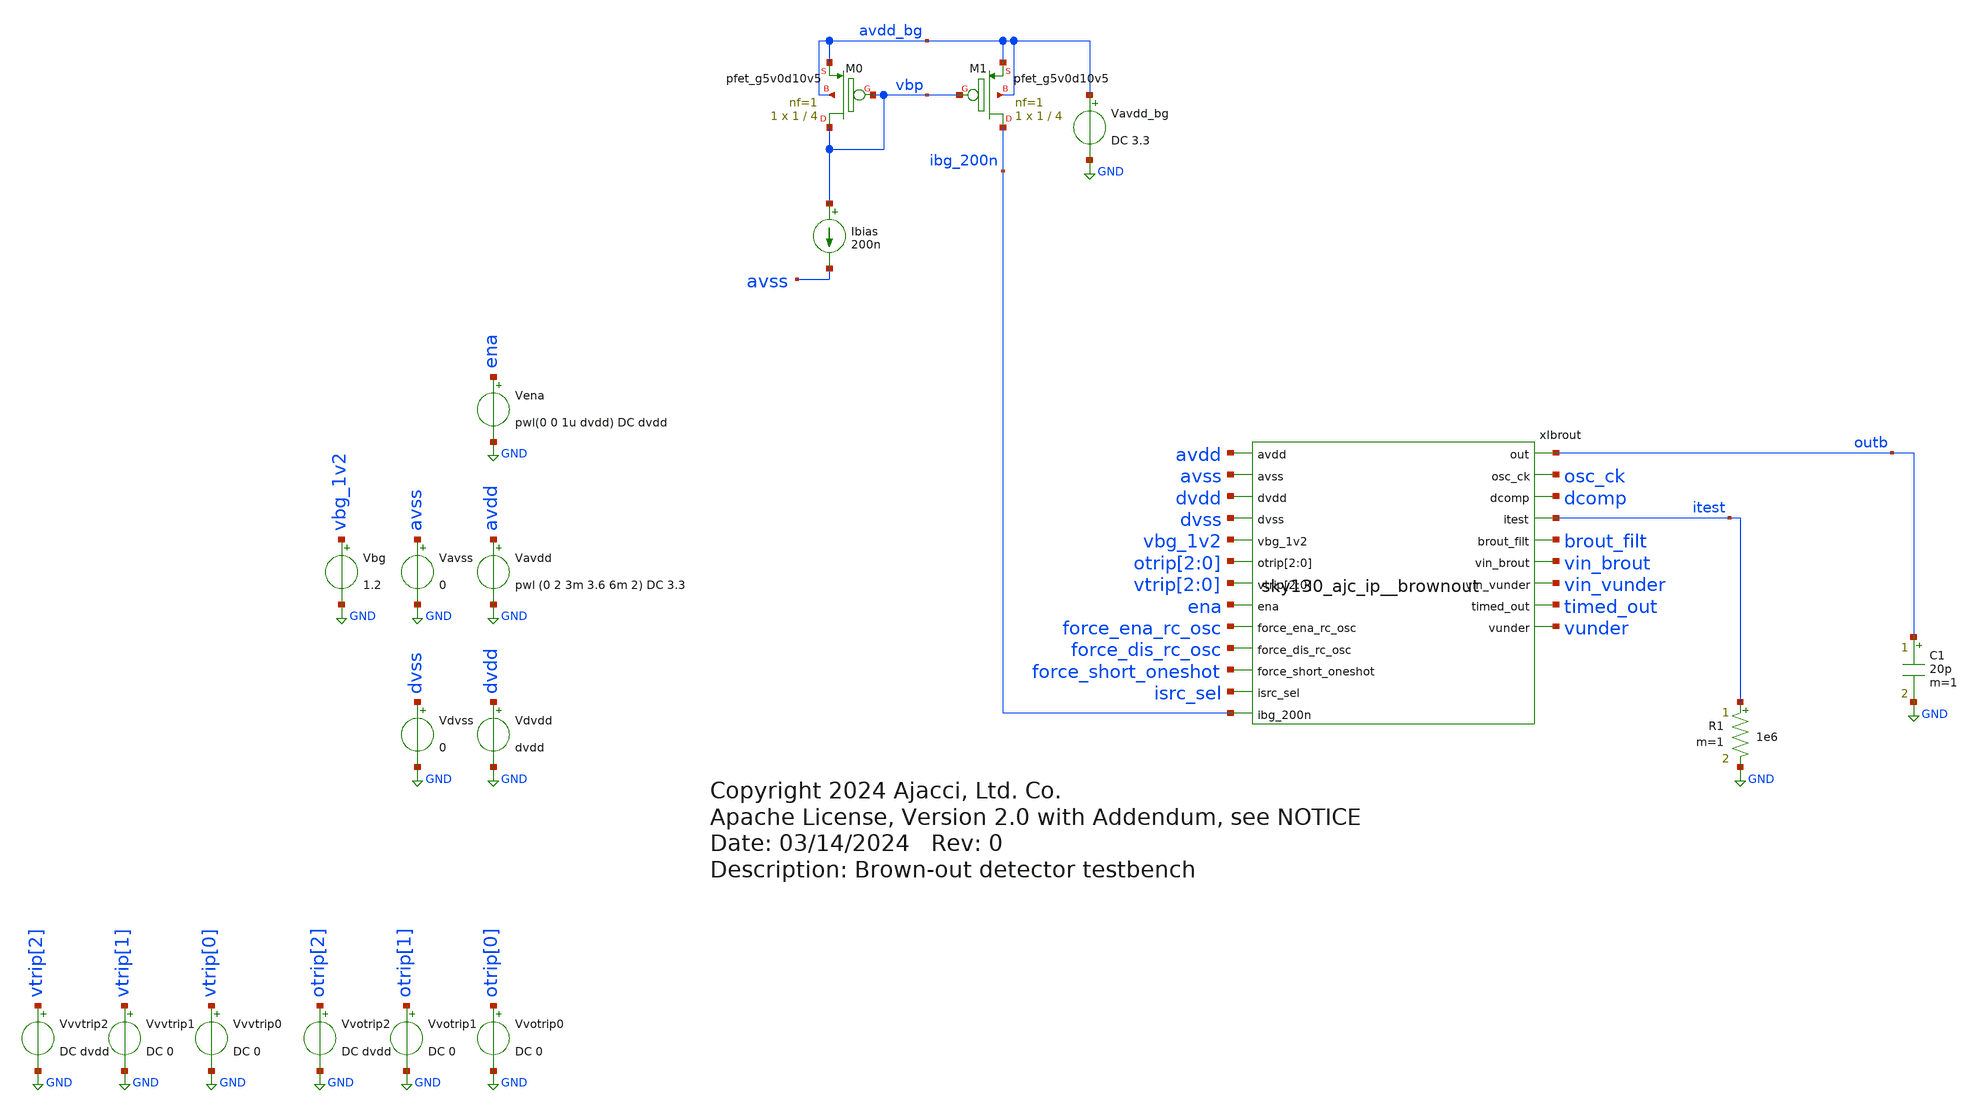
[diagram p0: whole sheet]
** sch_path: xschem/sky130_ajc_ip__brownout_tb.sch
* Copyright 2024 Ajacci, Ltd. Co.
* Apache License, Version 2.0 with Addendum, see NOTICE
**.subckt sky130_ajc_ip__brownout_tb
Vavss avss GND 0
Vena ena GND pwl(0 0 1u dvdd) DC dvdd
Vavdd avdd GND pwl (0 2 3m 3.6 6m 2) DC 3.3
.save i(vavdd)
Vbg vbg_1v2 GND 1.2
Ibias vbp avss 200n
XM1 ibg_200n vbp avdd_bg avdd_bg sky130_fd_pr__pfet_g5v0d10v5 L=4 W=1 nf=1 ad='int((nf+1)/2) * W/nf * 0.29'
+ as='int((nf+2)/2) * W/nf * 0.29' pd='2*int((nf+1)/2) * (W/nf + 0.29)' ps='2*int((nf+2)/2) * (W/nf + 0.29)'
+ nrd='0.29 / W' nrs='0.29 / W' sa=0 sb=0 sd=0 mult=1 m=1
XM0 vbp vbp avdd_bg avdd_bg sky130_fd_pr__pfet_g5v0d10v5 L=4 W=1 nf=1 ad='int((nf+1)/2) * W/nf * 0.29'
+ as='int((nf+2)/2) * W/nf * 0.29' pd='2*int((nf+1)/2) * (W/nf + 0.29)' ps='2*int((nf+2)/2) * (W/nf + 0.29)'
+ nrd='0.29 / W' nrs='0.29 / W' sa=0 sb=0 sd=0 mult=1 m=1
Vdvss dvss GND 0
Vdvdd dvdd GND dvdd
.save i(vdvdd)
R1 itest GND 1e6 m=1
C1 outb GND 20p m=1
xIbrout avdd avss outb dvdd osc_ck dvss dcomp vbg_1v2 otrip[2] otrip[1] otrip[0] itest brout_filt
+ vtrip[2] vtrip[1] vtrip[0] vin_brout ena force_ena_rc_osc vin_vunder force_dis_rc_osc timed_out vunder
+ force_short_oneshot isrc_sel ibg_200n sky130_ajc_ip__brownout
Vvotrip0 otrip[0] GND DC 0
Vvotrip1 otrip[1] GND DC 0
Vvotrip2 otrip[2] GND DC dvdd
Vvvtrip0 vtrip[0] GND DC 0
Vvvtrip1 vtrip[1] GND DC 0
.save i(vvvtrip1)
Vvvtrip2 vtrip[2] GND DC dvdd
Vavdd_bg avdd_bg GND DC 3.3
**** begin user architecture code


.param avdd=3.3
.param dvdd=1.8
*.csparam dvdd2=dvdd/2
.csparam=0.9
.lib /usr/local/share/pdk/sky130A/libs.tech/ngspice/sky130.lib.spice tt
.include /usr/local/share/pdk/sky130A/libs.ref/sky130_fd_sc_hvl/spice/sky130_fd_sc_hvl.spice
.include /usr/local/share/pdk/sky130A/libs.ref/sky130_fd_sc_hd/spice/sky130_fd_sc_hd.spice

*dig pull up/down to set test bits
R000 ena dvdd 1e6
R001 force_ena_rc_osc dvss 1e6
R002 force_dis_rc_osc dvdd 1e6
R003 force_short_oneshot dvdd 1e6
R004 isrc_sel dvss 1e6

.option reltol=5e-5
.temp 25
.save all
.save @m.xibrout.xiana.xirsmux.xmena.msky130_fd_pr__nfet_g5v0d10v5[id]
.control
*op
tran 10u 6m
*meas tran otrip_r find v(avdd) when v(brout_filt)=$&dvdd2 td=300u rise=1
*meas tran otrip_f find v(avdd) when v(brout_filt)=$&dvdd2 td=300u fall=1
*meas tran vtrip_r find v(avdd) when v(vunder)=$&dvdd2 td=300u rise=1
*meas tran vtrip_f find v(avdd) when v(vunder)=$&dvdd2 td=300u fall=1
meas tran otrip_r find v(avdd) when v(brout_filt)=0.9 td=3m rise=1
meas tran otrip_f find v(avdd) when v(brout_filt)=0.9 td=300u fall=1
meas tran vtrip_r find v(avdd) when v(vunder)=0.9 td=300u rise=1
meas tran vtrip_f find v(avdd) when v(vunder)=0.9 td=3m fall=1

let hyst_br = $&otrip_f - $&otrip_r
let hyst_vu = $&vtrip_r - $&vtrip_f
print $&hyst_br
print $&hyst_vu

*let accu_br = ($&otrip_r + $&otrip_f)/2
*let accu_vu = ($&vtrip_r + $&vtrip_f)/2
*print $&accu_br
*print $&accu_vu

*plot @m.xibrout.xiana.xirsmux.xmena.msky130_fd_pr__nfet_g5v0d10v5[id]
plot 1.4*brout_filt avdd 1.5*vunder vbg_1v2 vin_brout
plot xibrout.xiana.xiosc.in osc_ck*1.1 xibrout.xiana.xiosc.net1*1.2 xibrout.xiana.xiosc.m*1.3
+ xibrout.xiana.xiosc.n*1.4

*plot brout_filt itest avdd ena vbg_1v2 vin_brout vin_vunder timed_out xibrout.xiana.dcomp
*+ xibrout.xiana.dcomp_filt
*plot i(Vavdd) i(Vdvdd)
*plot outb avdd vunder*0.75 ena*0.5
*plot xibrout.osc_ena 1.25*out 1.75*brout_filt
*plot 0.5*brout_filt 0.75*xibrout.xiana.dcomp xibrout.xiana.dcomp_filt
*plot avdd 0.25*osc_ck 0.5*ena 0.75*brout_filt timed_out 1.25*outb 1.5*vunder
*plot osc_ck*0.5 xibrout.xiana.xiosc.in xibrout.xiana.xiosc.m xibrout.osc_ena*0.25 brout_filt
*+ out*1.25
.endc


**** end user architecture code
**.ends
.GLOBAL GND
.end
